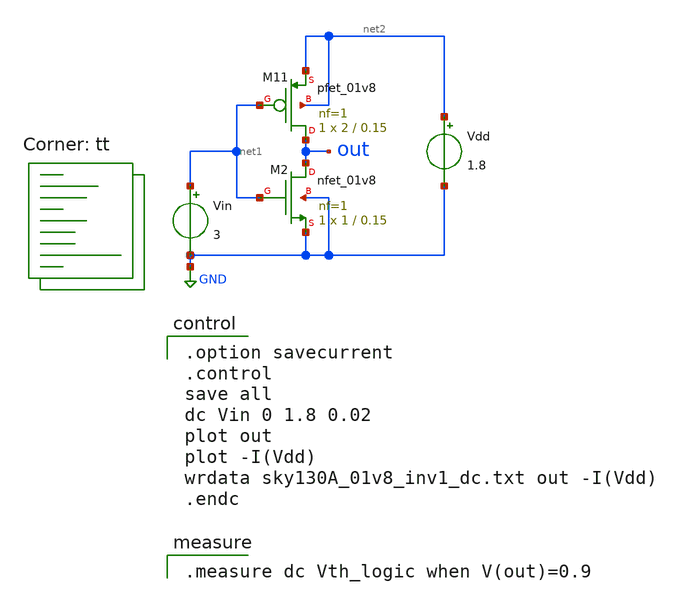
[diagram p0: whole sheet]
** sch_path: xschem/Logic/sky130A_01v8_inv1_dc.sch
* Copyright 2021 Stefan Frederik Schippers
* Licensed under the Apache License, Version 2.0 (the "License");
* you may not use this file except in compliance with the License.
* You may obtain a copy of the License at
* https://www.apache.org/licenses/LICENSE-2.0
* Unless required by applicable law or agreed to in writing, software
* distributed under the License is distributed on an "AS IS" BASIS,
* WITHOUT WARRANTIES OR CONDITIONS OF ANY KIND, either express or implied.
* See the License for the specific language governing permissions and
* limitations under the License.
**.subckt sky130A_01v8_inv1_dc
Vin net1 GND 3
Vdd net2 GND 1.8
XM11 out net1 net2 net2 sky130_fd_pr__pfet_01v8 L=0.15 W=2 nf=1 ad='int((nf+1)/2) * W/nf * 0.29' as='int((nf+2)/2) * W/nf * 0.29'
+ pd='2*int((nf+1)/2) * (W/nf + 0.29)' ps='2*int((nf+2)/2) * (W/nf + 0.29)' nrd='0.29 / W' nrs='0.29 / W'
+ sa=0 sb=0 sd=0 mult=1 m=1
XM2 out net1 GND GND sky130_fd_pr__nfet_01v8 L=0.15 W=1 nf=1 ad='int((1 + 1)/2) * 1 / 1 * 0.29' as='int((1 + 2)/2) * 1 / 1 * 0.29'
+ pd='2*int((1 + 1)/2) * (1 / 1 + 0.29)' ps='2*int((1 + 2)/2) * (1 / 1 + 0.29)' nrd='0.29 / 1 ' nrs='0.29 / 1 '
+ sa=0 sb=0 sd=0 mult=1 m=1
**** begin user architecture code
.lib $::SKYWATER_MODELS/sky130.lib.spice tt

.option savecurrent
.control
save all
dc Vin 0 1.8 0.02
plot out
plot -I(Vdd)
wrdata sky130A_01v8_inv1_dc.txt out -I(Vdd)
.endc


.measure dc Vth_logic when V(out)=0.9

**** end user architecture code
**.ends
.GLOBAL GND
.end
